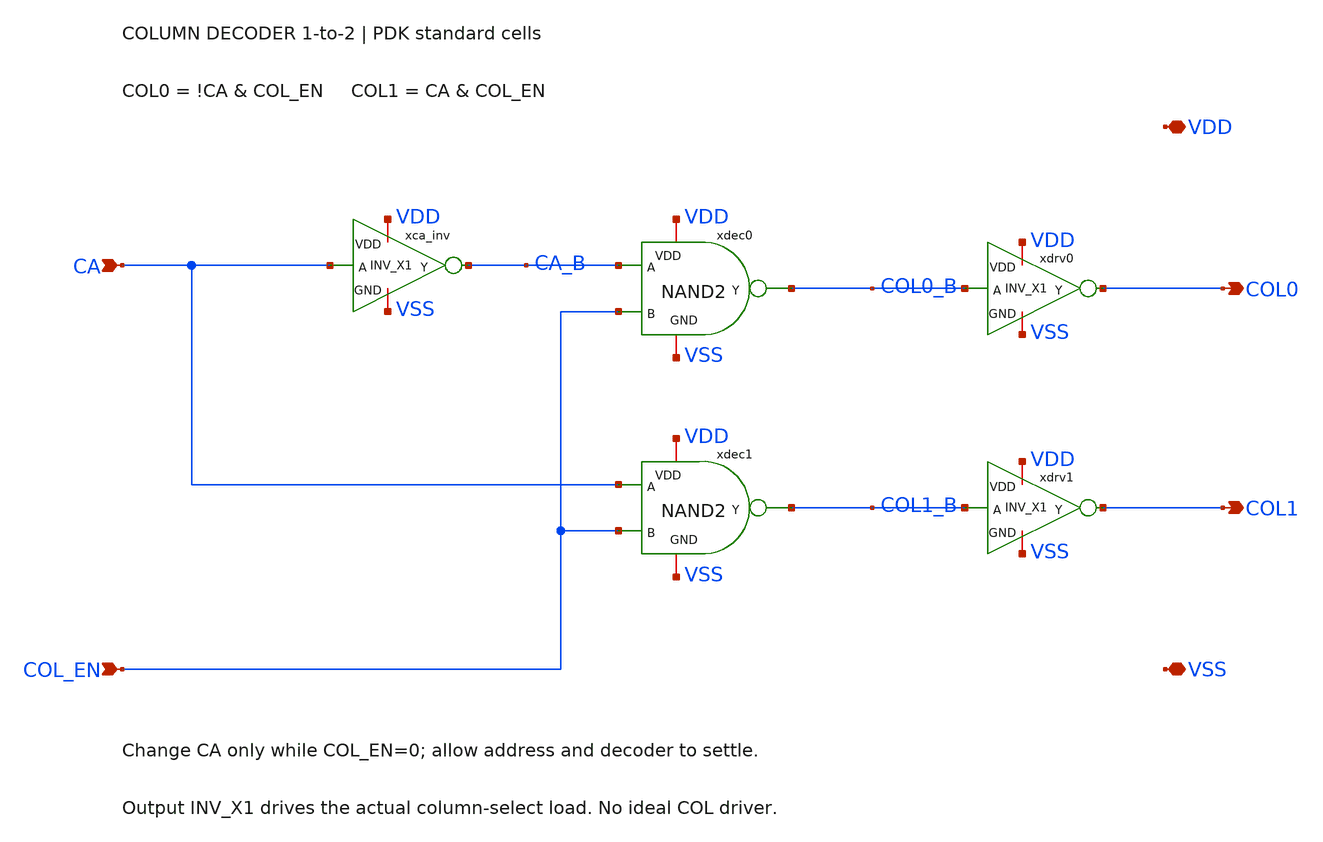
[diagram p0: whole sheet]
** sch_path: col_decoder_1to2.sch
**.subckt col_decoder_1to2 CA COL_EN COL0 COL1 VDD VSS
*.ipin CA
*.ipin COL_EN
*.opin COL0
*.opin COL1
*.iopin VDD
*.iopin VSS
xca_inv VDD CA CA_B VSS INV_X1
xdec0 VDD COL0_B CA_B COL_EN VSS NAND2
xdrv0 VDD COL0_B COL0 VSS INV_X1
xdec1 VDD COL1_B CA COL_EN VSS NAND2
xdrv1 VDD COL1_B COL1 VSS INV_X1
**.ends
.end
